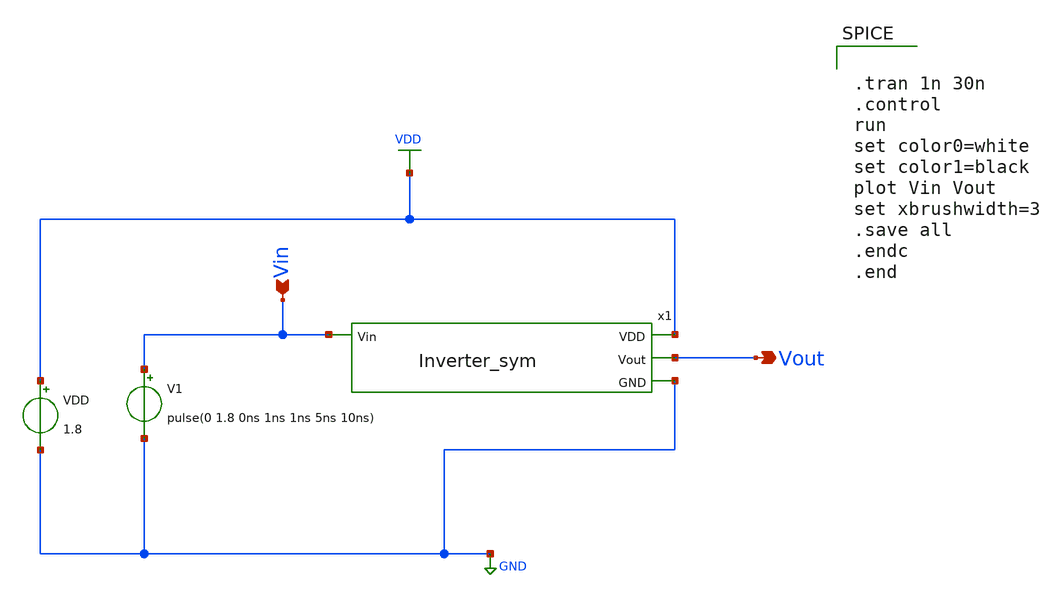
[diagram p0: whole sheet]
** sch_path: Week_0/Inverter_PreLayout/Inverter_tb.sch
**.subckt Inverter_tb Vin Vout
*.ipin Vin
*.opin Vout
V1 Vin GND pulse(0 1.8 0ns 1ns 1ns 5ns 10ns)
VDD VDD GND 1.8
x1 VDD Vout Vin GND Inverter_sym
**** begin user architecture code


.lib /home/swagatika/open_pdks/sky130/sky130A/libs.tech/ngspice/sky130.lib.spice tt

.save all





.tran 1n 30n
.control
run
set color0=white
set color1=black
plot Vin Vout
set xbrushwidth=3
.save all
.endc
.end


**** end user architecture code
**.ends

* expanding   symbol:  /home/swagatika/Desktop/Circuits/Inverter_sym.sym # of pins=4
** sym_path: Week_0/Inverter_PreLayout/Inverter_sym.sym
** sch_path: Week_0/Inverter_PreLayout/Inverter_sym.sch
.subckt Inverter_sym vdd OUT IN gnd
*.opin OUT
*.ipin IN
*.iopin vdd
*.iopin gnd
XPMOS OUT IN vdd vdd sky130_fd_pr__pfet_01v8 L=0.15 W=1 nf=1 ad='int((nf+1)/2) * W/nf * 0.29' as='int((nf+2)/2) * W/nf * 0.29'
+ pd='2*int((nf+1)/2) * (W/nf + 0.29)' ps='2*int((nf+2)/2) * (W/nf + 0.29)' nrd='0.29 / W' nrs='0.29 / W'
+ sa=0 sb=0 sd=0 mult=1 m=1
XNMOS OUT IN gnd gnd sky130_fd_pr__nfet_01v8 L=0.15 W=1 nf=1 ad='int((nf+1)/2) * W/nf * 0.29' as='int((nf+2)/2) * W/nf * 0.29'
+ pd='2*int((nf+1)/2) * (W/nf + 0.29)' ps='2*int((nf+2)/2) * (W/nf + 0.29)' nrd='0.29 / W' nrs='0.29 / W'
+ sa=0 sb=0 sd=0 mult=1 m=1
.ends

.GLOBAL GND
.GLOBAL VDD
.end
